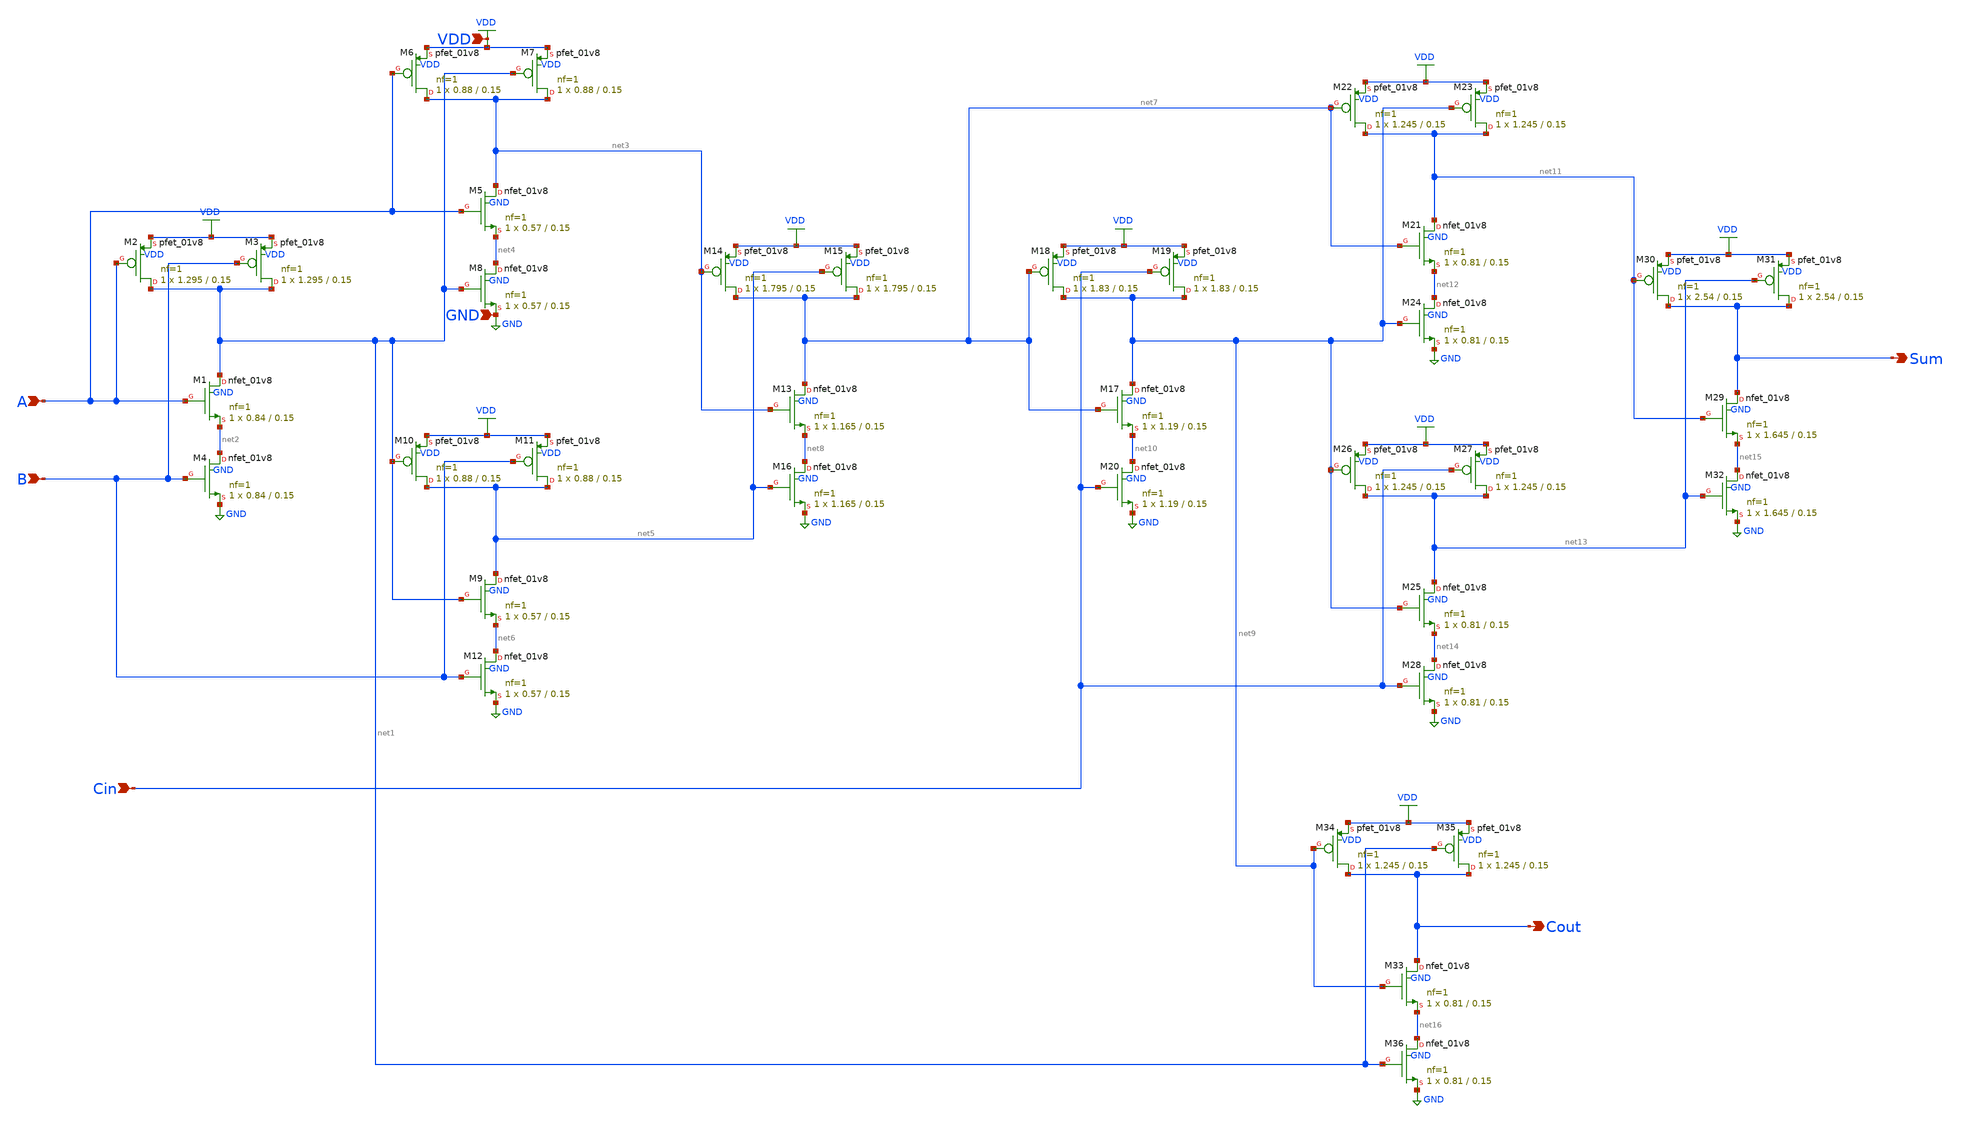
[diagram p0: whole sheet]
** sch_path: schematic/fulladder.sch
**.subckt fulladder A B Cin Cout Sum VDD GND
*.ipin A
*.ipin B
*.ipin Cin
*.opin Cout
*.opin Sum
*.ipin VDD
*.ipin GND
XM1 net1 A net2 GND sky130_fd_pr__nfet_01v8 L=0.15 W=0.84 nf=1 ad='int((1 + 1)/2) * 0.84 / 1 * 0.29'
+ as='int((1 + 2)/2) * 0.84 / 1 * 0.29' pd='2*int((1 + 1)/2) * (0.84 / 1 + 0.29)' ps='2*int((1 + 2)/2) * (0.84 / 1 + 0.29)'
+ nrd='0.29 / 0.84 ' nrs='0.29 / 0.84 ' sa=0 sb=0 sd=0 mult=1 m=1
XM2 net1 A VDD VDD sky130_fd_pr__pfet_01v8 L=0.15 W=1.295 nf=1 ad='int((1 + 1)/2) * 1.295 / 1 * 0.29'
+ as='int((1 + 2)/2) * 1.295 / 1 * 0.29' pd='2*int((1 + 1)/2) * (1.295 / 1 + 0.29)' ps='2*int((1 + 2)/2) * (1.295 / 1 + 0.29)'
+ nrd='0.29 / 1.295 ' nrs='0.29 / 1.295 ' sa=0 sb=0 sd=0 mult=1 m=1
XM3 net1 B VDD VDD sky130_fd_pr__pfet_01v8 L=0.15 W=1.295 nf=1 ad='int((1 + 1)/2) * 1.295 / 1 * 0.29'
+ as='int((1 + 2)/2) * 1.295 / 1 * 0.29' pd='2*int((1 + 1)/2) * (1.295 / 1 + 0.29)' ps='2*int((1 + 2)/2) * (1.295 / 1 + 0.29)'
+ nrd='0.29 / 1.295 ' nrs='0.29 / 1.295 ' sa=0 sb=0 sd=0 mult=1 m=1
XM4 net2 B GND GND sky130_fd_pr__nfet_01v8 L=0.15 W=0.84 nf=1 ad='int((1 + 1)/2) * 0.84 / 1 * 0.29' as='int((1 + 2)/2) * 0.84 / 1 * 0.29'
+ pd='2*int((1 + 1)/2) * (0.84 / 1 + 0.29)' ps='2*int((1 + 2)/2) * (0.84 / 1 + 0.29)' nrd='0.29 / 0.84 '
+ nrs='0.29 / 0.84 ' sa=0 sb=0 sd=0 mult=1 m=1
XM5 net3 A net4 GND sky130_fd_pr__nfet_01v8 L=0.15 W=0.57 nf=1 ad='int((1 + 1)/2) * 0.57 / 1 * 0.29'
+ as='int((1 + 2)/2) * 0.57 / 1 * 0.29' pd='2*int((1 + 1)/2) * (0.57 / 1 + 0.29)' ps='2*int((1 + 2)/2) * (0.57 / 1 + 0.29)'
+ nrd='0.29 / 0.57 ' nrs='0.29 / 0.57 ' sa=0 sb=0 sd=0 mult=1 m=1
XM6 net3 A VDD VDD sky130_fd_pr__pfet_01v8 L=0.15 W=0.88 nf=1 ad='int((1 + 1)/2) * 0.88 / 1 * 0.29' as='int((1 + 2)/2) * 0.88 / 1 * 0.29'
+ pd='2*int((1 + 1)/2) * (0.88 / 1 + 0.29)' ps='2*int((1 + 2)/2) * (0.88 / 1 + 0.29)' nrd='0.29 / 0.88 '
+ nrs='0.29 / 0.88 ' sa=0 sb=0 sd=0 mult=1 m=1
XM7 net3 net1 VDD VDD sky130_fd_pr__pfet_01v8 L=0.15 W=0.88 nf=1 ad='int((1 + 1)/2) * 0.88 / 1 * 0.29'
+ as='int((1 + 2)/2) * 0.88 / 1 * 0.29' pd='2*int((1 + 1)/2) * (0.88 / 1 + 0.29)' ps='2*int((1 + 2)/2) * (0.88 / 1 + 0.29)'
+ nrd='0.29 / 0.88 ' nrs='0.29 / 0.88 ' sa=0 sb=0 sd=0 mult=1 m=1
XM8 net4 net1 GND GND sky130_fd_pr__nfet_01v8 L=0.15 W=0.57 nf=1 ad='int((1 + 1)/2) * 0.57 / 1 * 0.29'
+ as='int((1 + 2)/2) * 0.57 / 1 * 0.29' pd='2*int((1 + 1)/2) * (0.57 / 1 + 0.29)' ps='2*int((1 + 2)/2) * (0.57 / 1 + 0.29)'
+ nrd='0.29 / 0.57 ' nrs='0.29 / 0.57 ' sa=0 sb=0 sd=0 mult=1 m=1
XM9 net5 net1 net6 GND sky130_fd_pr__nfet_01v8 L=0.15 W=0.57 nf=1 ad='int((1 + 1)/2) * 0.57 / 1 * 0.29'
+ as='int((1 + 2)/2) * 0.57 / 1 * 0.29' pd='2*int((1 + 1)/2) * (0.57 / 1 + 0.29)' ps='2*int((1 + 2)/2) * (0.57 / 1 + 0.29)'
+ nrd='0.29 / 0.57 ' nrs='0.29 / 0.57 ' sa=0 sb=0 sd=0 mult=1 m=1
XM10 net5 net1 VDD VDD sky130_fd_pr__pfet_01v8 L=0.15 W=0.88 nf=1 ad='int((1 + 1)/2) * 0.88 / 1 * 0.29'
+ as='int((1 + 2)/2) * 0.88 / 1 * 0.29' pd='2*int((1 + 1)/2) * (0.88 / 1 + 0.29)' ps='2*int((1 + 2)/2) * (0.88 / 1 + 0.29)'
+ nrd='0.29 / 0.88 ' nrs='0.29 / 0.88 ' sa=0 sb=0 sd=0 mult=1 m=1
XM11 net5 B VDD VDD sky130_fd_pr__pfet_01v8 L=0.15 W=0.88 nf=1 ad='int((1 + 1)/2) * 0.88 / 1 * 0.29'
+ as='int((1 + 2)/2) * 0.88 / 1 * 0.29' pd='2*int((1 + 1)/2) * (0.88 / 1 + 0.29)' ps='2*int((1 + 2)/2) * (0.88 / 1 + 0.29)'
+ nrd='0.29 / 0.88 ' nrs='0.29 / 0.88 ' sa=0 sb=0 sd=0 mult=1 m=1
XM12 net6 B GND GND sky130_fd_pr__nfet_01v8 L=0.15 W=0.57 nf=1 ad='int((1 + 1)/2) * 0.57 / 1 * 0.29'
+ as='int((1 + 2)/2) * 0.57 / 1 * 0.29' pd='2*int((1 + 1)/2) * (0.57 / 1 + 0.29)' ps='2*int((1 + 2)/2) * (0.57 / 1 + 0.29)'
+ nrd='0.29 / 0.57 ' nrs='0.29 / 0.57 ' sa=0 sb=0 sd=0 mult=1 m=1
XM13 net7 net3 net8 GND sky130_fd_pr__nfet_01v8 L=0.15 W=1.165 nf=1 ad='int((1 + 1)/2) * 1.165 / 1 * 0.29'
+ as='int((1 + 2)/2) * 1.165 / 1 * 0.29' pd='2*int((1 + 1)/2) * (1.165 / 1 + 0.29)' ps='2*int((1 + 2)/2) * (1.165 / 1 + 0.29)'
+ nrd='0.29 / 1.165 ' nrs='0.29 / 1.165 ' sa=0 sb=0 sd=0 mult=1 m=1
XM14 net7 net3 VDD VDD sky130_fd_pr__pfet_01v8 L=0.15 W=1.795 nf=1 ad='int((1 + 1)/2) * 1.795 / 1 * 0.29'
+ as='int((1 + 2)/2) * 1.795 / 1 * 0.29' pd='2*int((1 + 1)/2) * (1.795 / 1 + 0.29)' ps='2*int((1 + 2)/2) * (1.795 / 1 + 0.29)'
+ nrd='0.29 / 1.795 ' nrs='0.29 / 1.795 ' sa=0 sb=0 sd=0 mult=1 m=1
XM15 net7 net5 VDD VDD sky130_fd_pr__pfet_01v8 L=0.15 W=1.795 nf=1 ad='int((1 + 1)/2) * 1.795 / 1 * 0.29'
+ as='int((1 + 2)/2) * 1.795 / 1 * 0.29' pd='2*int((1 + 1)/2) * (1.795 / 1 + 0.29)' ps='2*int((1 + 2)/2) * (1.795 / 1 + 0.29)'
+ nrd='0.29 / 1.795 ' nrs='0.29 / 1.795 ' sa=0 sb=0 sd=0 mult=1 m=1
XM16 net8 net5 GND GND sky130_fd_pr__nfet_01v8 L=0.15 W=1.165 nf=1 ad='int((1 + 1)/2) * 1.165 / 1 * 0.29'
+ as='int((1 + 2)/2) * 1.165 / 1 * 0.29' pd='2*int((1 + 1)/2) * (1.165 / 1 + 0.29)' ps='2*int((1 + 2)/2) * (1.165 / 1 + 0.29)'
+ nrd='0.29 / 1.165 ' nrs='0.29 / 1.165 ' sa=0 sb=0 sd=0 mult=1 m=1
XM17 net9 net7 net10 GND sky130_fd_pr__nfet_01v8 L=0.15 W=1.19 nf=1 ad='int((1 + 1)/2) * 1.19 / 1 * 0.29'
+ as='int((1 + 2)/2) * 1.19 / 1 * 0.29' pd='2*int((1 + 1)/2) * (1.19 / 1 + 0.29)' ps='2*int((1 + 2)/2) * (1.19 / 1 + 0.29)'
+ nrd='0.29 / 1.19 ' nrs='0.29 / 1.19 ' sa=0 sb=0 sd=0 mult=1 m=1
XM18 net9 net7 VDD VDD sky130_fd_pr__pfet_01v8 L=0.15 W=1.83 nf=1 ad='int((1 + 1)/2) * 1.83 / 1 * 0.29'
+ as='int((1 + 2)/2) * 1.83 / 1 * 0.29' pd='2*int((1 + 1)/2) * (1.83 / 1 + 0.29)' ps='2*int((1 + 2)/2) * (1.83 / 1 + 0.29)'
+ nrd='0.29 / 1.83 ' nrs='0.29 / 1.83 ' sa=0 sb=0 sd=0 mult=1 m=1
XM19 net9 Cin VDD VDD sky130_fd_pr__pfet_01v8 L=0.15 W=1.83 nf=1 ad='int((1 + 1)/2) * 1.83 / 1 * 0.29'
+ as='int((1 + 2)/2) * 1.83 / 1 * 0.29' pd='2*int((1 + 1)/2) * (1.83 / 1 + 0.29)' ps='2*int((1 + 2)/2) * (1.83 / 1 + 0.29)'
+ nrd='0.29 / 1.83 ' nrs='0.29 / 1.83 ' sa=0 sb=0 sd=0 mult=1 m=1
XM20 net10 Cin GND GND sky130_fd_pr__nfet_01v8 L=0.15 W=1.19 nf=1 ad='int((1 + 1)/2) * 1.19 / 1 * 0.29'
+ as='int((1 + 2)/2) * 1.19 / 1 * 0.29' pd='2*int((1 + 1)/2) * (1.19 / 1 + 0.29)' ps='2*int((1 + 2)/2) * (1.19 / 1 + 0.29)'
+ nrd='0.29 / 1.19 ' nrs='0.29 / 1.19 ' sa=0 sb=0 sd=0 mult=1 m=1
XM21 net11 net7 net12 GND sky130_fd_pr__nfet_01v8 L=0.15 W=0.81 nf=1 ad='int((1 + 1)/2) * 0.81 / 1 * 0.29'
+ as='int((1 + 2)/2) * 0.81 / 1 * 0.29' pd='2*int((1 + 1)/2) * (0.81 / 1 + 0.29)' ps='2*int((1 + 2)/2) * (0.81 / 1 + 0.29)'
+ nrd='0.29 / 0.81 ' nrs='0.29 / 0.81 ' sa=0 sb=0 sd=0 mult=1 m=1
XM22 net11 net7 VDD VDD sky130_fd_pr__pfet_01v8 L=0.15 W=1.245 nf=1 ad='int((1 + 1)/2) * 1.245 / 1 * 0.29'
+ as='int((1 + 2)/2) * 1.245 / 1 * 0.29' pd='2*int((1 + 1)/2) * (1.245 / 1 + 0.29)' ps='2*int((1 + 2)/2) * (1.245 / 1 + 0.29)'
+ nrd='0.29 / 1.245 ' nrs='0.29 / 1.245 ' sa=0 sb=0 sd=0 mult=1 m=1
XM23 net11 net9 VDD VDD sky130_fd_pr__pfet_01v8 L=0.15 W=1.245 nf=1 ad='int((1 + 1)/2) * 1.245 / 1 * 0.29'
+ as='int((1 + 2)/2) * 1.245 / 1 * 0.29' pd='2*int((1 + 1)/2) * (1.245 / 1 + 0.29)' ps='2*int((1 + 2)/2) * (1.245 / 1 + 0.29)'
+ nrd='0.29 / 1.245 ' nrs='0.29 / 1.245 ' sa=0 sb=0 sd=0 mult=1 m=1
XM24 net12 net9 GND GND sky130_fd_pr__nfet_01v8 L=0.15 W=0.81 nf=1 ad='int((1 + 1)/2) * 0.81 / 1 * 0.29'
+ as='int((1 + 2)/2) * 0.81 / 1 * 0.29' pd='2*int((1 + 1)/2) * (0.81 / 1 + 0.29)' ps='2*int((1 + 2)/2) * (0.81 / 1 + 0.29)'
+ nrd='0.29 / 0.81 ' nrs='0.29 / 0.81 ' sa=0 sb=0 sd=0 mult=1 m=1
XM25 net13 net9 net14 GND sky130_fd_pr__nfet_01v8 L=0.15 W=0.81 nf=1 ad='int((1 + 1)/2) * 0.81 / 1 * 0.29'
+ as='int((1 + 2)/2) * 0.81 / 1 * 0.29' pd='2*int((1 + 1)/2) * (0.81 / 1 + 0.29)' ps='2*int((1 + 2)/2) * (0.81 / 1 + 0.29)'
+ nrd='0.29 / 0.81 ' nrs='0.29 / 0.81 ' sa=0 sb=0 sd=0 mult=1 m=1
XM26 net13 net9 VDD VDD sky130_fd_pr__pfet_01v8 L=0.15 W=1.245 nf=1 ad='int((1 + 1)/2) * 1.245 / 1 * 0.29'
+ as='int((1 + 2)/2) * 1.245 / 1 * 0.29' pd='2*int((1 + 1)/2) * (1.245 / 1 + 0.29)' ps='2*int((1 + 2)/2) * (1.245 / 1 + 0.29)'
+ nrd='0.29 / 1.245 ' nrs='0.29 / 1.245 ' sa=0 sb=0 sd=0 mult=1 m=1
XM27 net13 Cin VDD VDD sky130_fd_pr__pfet_01v8 L=0.15 W=1.245 nf=1 ad='int((1 + 1)/2) * 1.245 / 1 * 0.29'
+ as='int((1 + 2)/2) * 1.245 / 1 * 0.29' pd='2*int((1 + 1)/2) * (1.245 / 1 + 0.29)' ps='2*int((1 + 2)/2) * (1.245 / 1 + 0.29)'
+ nrd='0.29 / 1.245 ' nrs='0.29 / 1.245 ' sa=0 sb=0 sd=0 mult=1 m=1
XM28 net14 Cin GND GND sky130_fd_pr__nfet_01v8 L=0.15 W=0.81 nf=1 ad='int((1 + 1)/2) * 0.81 / 1 * 0.29'
+ as='int((1 + 2)/2) * 0.81 / 1 * 0.29' pd='2*int((1 + 1)/2) * (0.81 / 1 + 0.29)' ps='2*int((1 + 2)/2) * (0.81 / 1 + 0.29)'
+ nrd='0.29 / 0.81 ' nrs='0.29 / 0.81 ' sa=0 sb=0 sd=0 mult=1 m=1
XM29 Sum net11 net15 GND sky130_fd_pr__nfet_01v8 L=0.15 W=1.645 nf=1 ad='int((1 + 1)/2) * 1.645 / 1 * 0.29'
+ as='int((1 + 2)/2) * 1.645 / 1 * 0.29' pd='2*int((1 + 1)/2) * (1.645 / 1 + 0.29)' ps='2*int((1 + 2)/2) * (1.645 / 1 + 0.29)'
+ nrd='0.29 / 1.645 ' nrs='0.29 / 1.645 ' sa=0 sb=0 sd=0 mult=1 m=1
XM30 Sum net11 VDD VDD sky130_fd_pr__pfet_01v8 L=0.15 W=2.54 nf=1 ad='int((1 + 1)/2) * 2.54 / 1 * 0.29'
+ as='int((1 + 2)/2) * 2.54 / 1 * 0.29' pd='2*int((1 + 1)/2) * (2.54 / 1 + 0.29)' ps='2*int((1 + 2)/2) * (2.54 / 1 + 0.29)'
+ nrd='0.29 / 2.54 ' nrs='0.29 / 2.54 ' sa=0 sb=0 sd=0 mult=1 m=1
XM31 Sum net13 VDD VDD sky130_fd_pr__pfet_01v8 L=0.15 W=2.54 nf=1 ad='int((1 + 1)/2) * 2.54 / 1 * 0.29'
+ as='int((1 + 2)/2) * 2.54 / 1 * 0.29' pd='2*int((1 + 1)/2) * (2.54 / 1 + 0.29)' ps='2*int((1 + 2)/2) * (2.54 / 1 + 0.29)'
+ nrd='0.29 / 2.54 ' nrs='0.29 / 2.54 ' sa=0 sb=0 sd=0 mult=1 m=1
XM32 net15 net13 GND GND sky130_fd_pr__nfet_01v8 L=0.15 W=1.645 nf=1 ad='int((1 + 1)/2) * 1.645 / 1 * 0.29'
+ as='int((1 + 2)/2) * 1.645 / 1 * 0.29' pd='2*int((1 + 1)/2) * (1.645 / 1 + 0.29)' ps='2*int((1 + 2)/2) * (1.645 / 1 + 0.29)'
+ nrd='0.29 / 1.645 ' nrs='0.29 / 1.645 ' sa=0 sb=0 sd=0 mult=1 m=1
XM33 Cout net9 net16 GND sky130_fd_pr__nfet_01v8 L=0.15 W=0.81 nf=1 ad='int((1 + 1)/2) * 0.81 / 1 * 0.29'
+ as='int((1 + 2)/2) * 0.81 / 1 * 0.29' pd='2*int((1 + 1)/2) * (0.81 / 1 + 0.29)' ps='2*int((1 + 2)/2) * (0.81 / 1 + 0.29)'
+ nrd='0.29 / 0.81 ' nrs='0.29 / 0.81 ' sa=0 sb=0 sd=0 mult=1 m=1
XM34 Cout net9 VDD VDD sky130_fd_pr__pfet_01v8 L=0.15 W=1.245 nf=1 ad='int((1 + 1)/2) * 1.245 / 1 * 0.29'
+ as='int((1 + 2)/2) * 1.245 / 1 * 0.29' pd='2*int((1 + 1)/2) * (1.245 / 1 + 0.29)' ps='2*int((1 + 2)/2) * (1.245 / 1 + 0.29)'
+ nrd='0.29 / 1.245 ' nrs='0.29 / 1.245 ' sa=0 sb=0 sd=0 mult=1 m=1
XM35 Cout net1 VDD VDD sky130_fd_pr__pfet_01v8 L=0.15 W=1.245 nf=1 ad='int((1 + 1)/2) * 1.245 / 1 * 0.29'
+ as='int((1 + 2)/2) * 1.245 / 1 * 0.29' pd='2*int((1 + 1)/2) * (1.245 / 1 + 0.29)' ps='2*int((1 + 2)/2) * (1.245 / 1 + 0.29)'
+ nrd='0.29 / 1.245 ' nrs='0.29 / 1.245 ' sa=0 sb=0 sd=0 mult=1 m=1
XM36 net16 net1 GND GND sky130_fd_pr__nfet_01v8 L=0.15 W=0.81 nf=1 ad='int((1 + 1)/2) * 0.81 / 1 * 0.29'
+ as='int((1 + 2)/2) * 0.81 / 1 * 0.29' pd='2*int((1 + 1)/2) * (0.81 / 1 + 0.29)' ps='2*int((1 + 2)/2) * (0.81 / 1 + 0.29)'
+ nrd='0.29 / 0.81 ' nrs='0.29 / 0.81 ' sa=0 sb=0 sd=0 mult=1 m=1
**.ends
.GLOBAL GND
.GLOBAL VDD
.end
